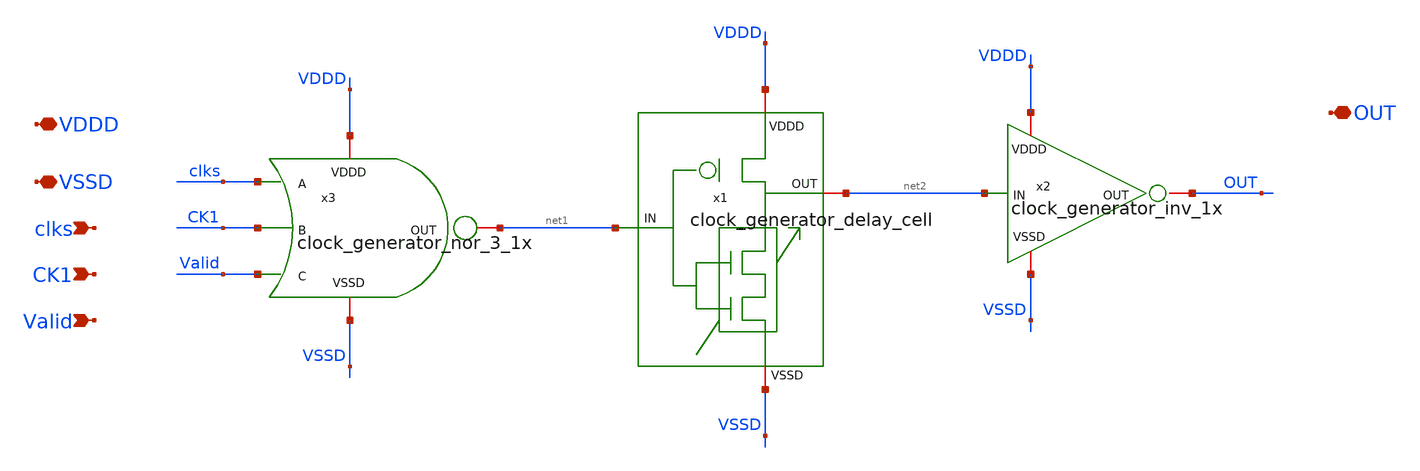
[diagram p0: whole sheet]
** sch_path: SAR_ADC/blocks/SAR_clock/clock_generator.sch
**.subckt clock_generator VDDD VSSD OUT clks CK1 Valid
*.iopin VDDD
*.iopin VSSD
*.iopin OUT
*.ipin clks
*.ipin CK1
*.ipin Valid
x1 VDDD VSSD net2 net1 clock_generator_delay_cell
x2 VDDD OUT VSSD net2 clock_generator_inv_1x
x3 VDDD net1 VSSD clks CK1 Valid clock_generator_nor_3_1x
**.ends

* expanding   symbol:
*+  /home/electrica/Documents/gf180_projects/gf180_work/PICO_contest/SAR_clock/clock_generator_delay_cell.sym # of pins=4
** sym_path: SAR_ADC/blocks/SAR_clock/clock_generator_delay_cell.sym
** sch_path: SAR_ADC/blocks/SAR_clock/clock_generator_delay_cell.sch
.subckt clock_generator_delay_cell VDDD VSSD OUT IN
*.iopin VDDD
*.iopin VSSD
*.ipin IN
*.iopin OUT
XM1 net1 IN VSSD VSSD nfet_03v3 L=2u W=0.22u nf=1 ad='int((nf+1)/2) * W/nf * 0.18u' as='int((nf+2)/2) * W/nf * 0.18u'
+ pd='2*int((nf+1)/2) * (W/nf + 0.18u)' ps='2*int((nf+2)/2) * (W/nf + 0.18u)' nrd='0.18u / W' nrs='0.18u / W'
+ sa=0 sb=0 sd=0 m=1
XM2 OUT IN net1 VSSD nfet_03v3 L=2u W=0.22u nf=1 ad='int((nf+1)/2) * W/nf * 0.18u' as='int((nf+2)/2) * W/nf * 0.18u'
+ pd='2*int((nf+1)/2) * (W/nf + 0.18u)' ps='2*int((nf+2)/2) * (W/nf + 0.18u)' nrd='0.18u / W' nrs='0.18u / W'
+ sa=0 sb=0 sd=0 m=1
XM3 OUT IN VDDD VDDD pfet_03v3 L=0.28u W=0.66u nf=1 ad='int((nf+1)/2) * W/nf * 0.18u' as='int((nf+2)/2) * W/nf * 0.18u'
+ pd='2*int((nf+1)/2) * (W/nf + 0.18u)' ps='2*int((nf+2)/2) * (W/nf + 0.18u)' nrd='0.18u / W' nrs='0.18u / W'
+ sa=0 sb=0 sd=0 m=1
.ends


* expanding   symbol:
*+  /home/electrica/Documents/gf180_projects/gf180_work/PICO_contest/SAR_clock/clock_generator_inv_1x.sym # of pins=4
** sym_path: SAR_ADC/SAR_clock/xschem/clock_generator_inv_1x.sym
** sch_path: SAR_ADC/SAR_clock/xschem/clock_generator_inv_1x.sch
.subckt clock_generator_inv_1x VDDD OUT VSSD IN
*.iopin VDDD
*.iopin VSSD
*.iopin OUT
*.ipin IN
XM1 OUT IN VDDD VDDD pfet_03v3 L=0.28u W=3.9u nf=1 ad='int((nf+1)/2) * W/nf * 0.18u' as='int((nf+2)/2) * W/nf * 0.18u'
+ pd='2*int((nf+1)/2) * (W/nf + 0.18u)' ps='2*int((nf+2)/2) * (W/nf + 0.18u)' nrd='0.18u / W' nrs='0.18u / W'
+ sa=0 sb=0 sd=0 m=1
XM2 OUT IN VSSD VSSD nfet_03v3 L=0.28u W=1.56u nf=1 ad='int((nf+1)/2) * W/nf * 0.18u' as='int((nf+2)/2) * W/nf * 0.18u'
+ pd='2*int((nf+1)/2) * (W/nf + 0.18u)' ps='2*int((nf+2)/2) * (W/nf + 0.18u)' nrd='0.18u / W' nrs='0.18u / W'
+ sa=0 sb=0 sd=0 m=1
.ends


* expanding   symbol:
*+  /home/electrica/Documents/gf180_projects/gf180_work/PICO_contest/SAR_clock/clock_generator_nor_3_1x.sym # of pins=6
** sym_path: SAR_ADC/blocks/SAR_clock/clock_generator_nor_3_1x.sym
** sch_path: SAR_ADC/blocks/SAR_clock/clock_generator_nor_3_1x.sch
.subckt clock_generator_nor_3_1x VDDD OUT VSSD A B C
*.iopin VDDD
*.iopin VSSD
*.iopin OUT
*.ipin A
*.ipin B
*.ipin C
XM1 OUT B VSSD VSSD nfet_03v3 L=0.28u W=0.22u nf=1 ad='int((nf+1)/2) * W/nf * 0.18u' as='int((nf+2)/2) * W/nf * 0.18u'
+ pd='2*int((nf+1)/2) * (W/nf + 0.18u)' ps='2*int((nf+2)/2) * (W/nf + 0.18u)' nrd='0.18u / W' nrs='0.18u / W'
+ sa=0 sb=0 sd=0 m=1
XM2 OUT A VSSD VSSD nfet_03v3 L=0.28u W=0.22u nf=1 ad='int((nf+1)/2) * W/nf * 0.18u' as='int((nf+2)/2) * W/nf * 0.18u'
+ pd='2*int((nf+1)/2) * (W/nf + 0.18u)' ps='2*int((nf+2)/2) * (W/nf + 0.18u)' nrd='0.18u / W' nrs='0.18u / W'
+ sa=0 sb=0 sd=0 m=1
XM3 OUT C VSSD VSSD nfet_03v3 L=0.28u W=0.22u nf=1 ad='int((nf+1)/2) * W/nf * 0.18u' as='int((nf+2)/2) * W/nf * 0.18u'
+ pd='2*int((nf+1)/2) * (W/nf + 0.18u)' ps='2*int((nf+2)/2) * (W/nf + 0.18u)' nrd='0.18u / W' nrs='0.18u / W'
+ sa=0 sb=0 sd=0 m=1
XM4 OUT C net1 VDDD pfet_03v3 L=0.28u W=0.66u nf=1 ad='int((nf+1)/2) * W/nf * 0.18u' as='int((nf+2)/2) * W/nf * 0.18u'
+ pd='2*int((nf+1)/2) * (W/nf + 0.18u)' ps='2*int((nf+2)/2) * (W/nf + 0.18u)' nrd='0.18u / W' nrs='0.18u / W'
+ sa=0 sb=0 sd=0 m=1
XM5 net1 B net2 VDDD pfet_03v3 L=0.28u W=0.66u nf=1 ad='int((nf+1)/2) * W/nf * 0.18u' as='int((nf+2)/2) * W/nf * 0.18u'
+ pd='2*int((nf+1)/2) * (W/nf + 0.18u)' ps='2*int((nf+2)/2) * (W/nf + 0.18u)' nrd='0.18u / W' nrs='0.18u / W'
+ sa=0 sb=0 sd=0 m=1
XM6 net2 A VDDD VDDD pfet_03v3 L=0.28u W=0.66u nf=1 ad='int((nf+1)/2) * W/nf * 0.18u' as='int((nf+2)/2) * W/nf * 0.18u'
+ pd='2*int((nf+1)/2) * (W/nf + 0.18u)' ps='2*int((nf+2)/2) * (W/nf + 0.18u)' nrd='0.18u / W' nrs='0.18u / W'
+ sa=0 sb=0 sd=0 m=1
.ends

.end
